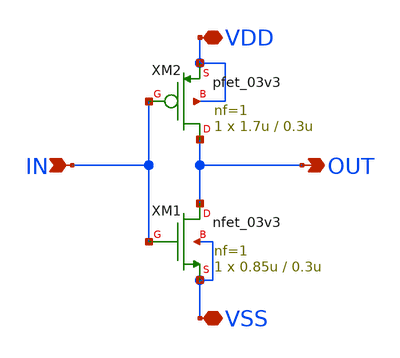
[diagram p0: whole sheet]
** sch_path: designs/cells/sdffrnq/sch/inv.sch
**.subckt inv IN OUT VDD VSS
*.ipin IN
*.opin OUT
*.iopin VDD
*.iopin VSS
XM2 OUT IN VDD VDD pfet_03v3 L=0.3u W=1.7u nf=1 ad='int((nf+1)/2) * W/nf * 0.18u' as='int((nf+2)/2) * W/nf * 0.18u'
+ pd='2*int((nf+1)/2) * (W/nf + 0.18u)' ps='2*int((nf+2)/2) * (W/nf + 0.18u)' nrd='0.18u / W' nrs='0.18u / W'
+ sa=0 sb=0 sd=0 m=1
XM1 OUT IN VSS VSS nfet_03v3 L=0.3u W=0.85u nf=1 ad='int((nf+1)/2) * W/nf * 0.18u' as='int((nf+2)/2) * W/nf * 0.18u'
+ pd='2*int((nf+1)/2) * (W/nf + 0.18u)' ps='2*int((nf+2)/2) * (W/nf + 0.18u)' nrd='0.18u / W' nrs='0.18u / W'
+ sa=0 sb=0 sd=0 m=1
**.ends
.end
